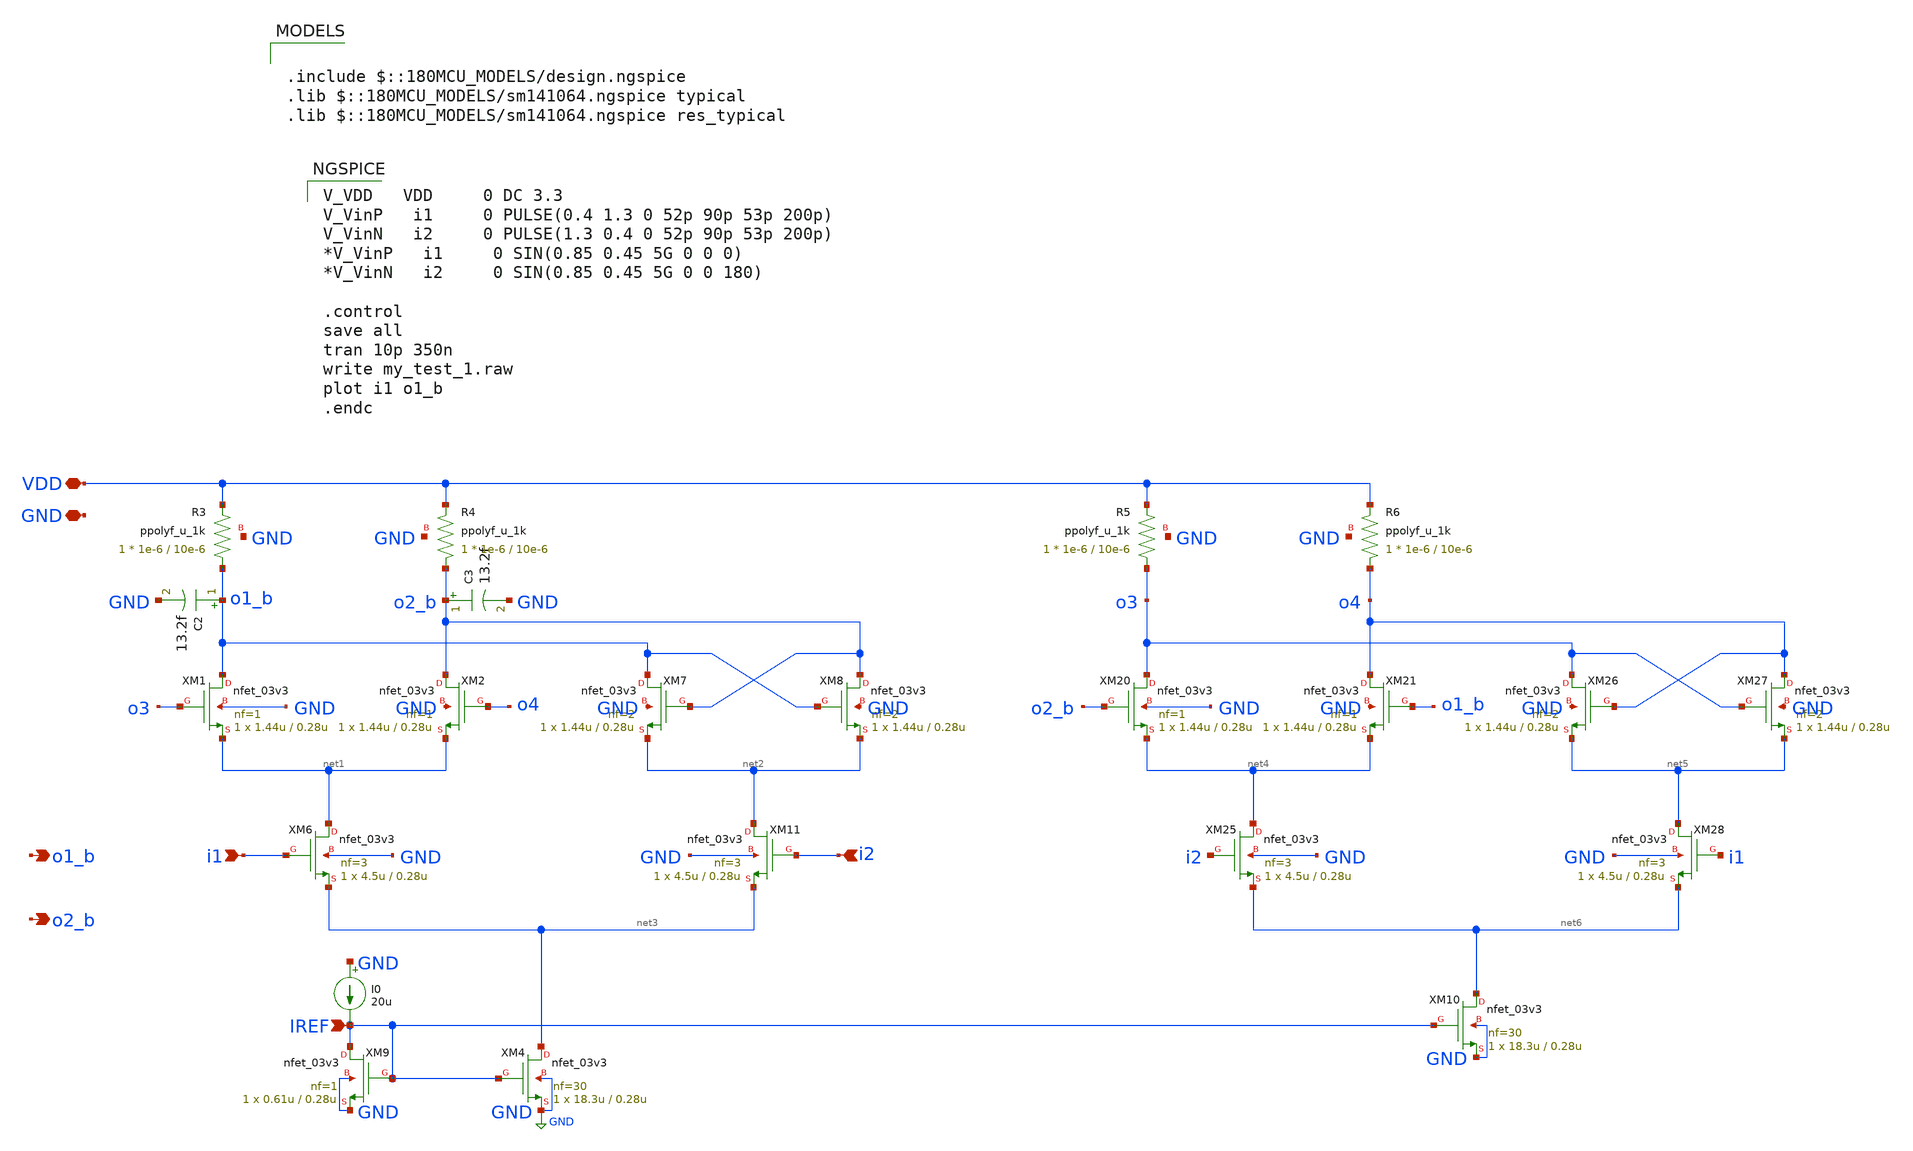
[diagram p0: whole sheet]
** sch_path: rha-vga-pll-blocks/blocks/pll/cml_div.sch
**.subckt cml_div i2 i1 o2_b o1_b VDD GND IREF
*.ipin i2
*.ipin i1
*.opin o2_b
*.opin o1_b
*.iopin VDD
*.iopin GND
*.ipin IREF
XM1 o1_b o3 net1 GND nfet_03v3 L=0.28u W=1.44u nf=1 ad='int((nf+1)/2) * W/nf * 0.18u' as='int((nf+2)/2) * W/nf * 0.18u'
+ pd='2*int((nf+1)/2) * (W/nf + 0.18u)' ps='2*int((nf+2)/2) * (W/nf + 0.18u)' nrd='0.18u / W' nrs='0.18u / W'
+ sa=0 sb=0 sd=0 m=1
XM2 o2_b o4 net1 GND nfet_03v3 L=0.28u W=1.44u nf=1 ad='int((nf+1)/2) * W/nf * 0.18u' as='int((nf+2)/2) * W/nf * 0.18u'
+ pd='2*int((nf+1)/2) * (W/nf + 0.18u)' ps='2*int((nf+2)/2) * (W/nf + 0.18u)' nrd='0.18u / W' nrs='0.18u / W'
+ sa=0 sb=0 sd=0 m=1
XM4 net3 IREF GND GND nfet_03v3 L=0.28u W=18.3u nf=30 ad='int((nf+1)/2) * W/nf * 0.18u' as='int((nf+2)/2) * W/nf * 0.18u'
+ pd='2*int((nf+1)/2) * (W/nf + 0.18u)' ps='2*int((nf+2)/2) * (W/nf + 0.18u)' nrd='0.18u / W' nrs='0.18u / W'
+ sa=0 sb=0 sd=0 m=1
XM6 net1 i1 net3 GND nfet_03v3 L=0.28u W=4.5u nf=3 ad='int((nf+1)/2) * W/nf * 0.18u' as='int((nf+2)/2) * W/nf * 0.18u'
+ pd='2*int((nf+1)/2) * (W/nf + 0.18u)' ps='2*int((nf+2)/2) * (W/nf + 0.18u)' nrd='0.18u / W' nrs='0.18u / W'
+ sa=0 sb=0 sd=0 m=1
XM7 o1_b o2_b net2 GND nfet_03v3 L=0.28u W=1.44u nf=2 ad='int((nf+1)/2) * W/nf * 0.18u' as='int((nf+2)/2) * W/nf * 0.18u'
+ pd='2*int((nf+1)/2) * (W/nf + 0.18u)' ps='2*int((nf+2)/2) * (W/nf + 0.18u)' nrd='0.18u / W' nrs='0.18u / W'
+ sa=0 sb=0 sd=0 m=1
XM8 o2_b o1_b net2 GND nfet_03v3 L=0.28u W=1.44u nf=2 ad='int((nf+1)/2) * W/nf * 0.18u' as='int((nf+2)/2) * W/nf * 0.18u'
+ pd='2*int((nf+1)/2) * (W/nf + 0.18u)' ps='2*int((nf+2)/2) * (W/nf + 0.18u)' nrd='0.18u / W' nrs='0.18u / W'
+ sa=0 sb=0 sd=0 m=1
XM11 net2 i2 net3 GND nfet_03v3 L=0.28u W=4.5u nf=3 ad='int((nf+1)/2) * W/nf * 0.18u' as='int((nf+2)/2) * W/nf * 0.18u'
+ pd='2*int((nf+1)/2) * (W/nf + 0.18u)' ps='2*int((nf+2)/2) * (W/nf + 0.18u)' nrd='0.18u / W' nrs='0.18u / W'
+ sa=0 sb=0 sd=0 m=1
XM9 IREF IREF GND GND nfet_03v3 L=0.28u W=0.61u nf=1 ad='int((nf+1)/2) * W/nf * 0.18u' as='int((nf+2)/2) * W/nf * 0.18u'
+ pd='2*int((nf+1)/2) * (W/nf + 0.18u)' ps='2*int((nf+2)/2) * (W/nf + 0.18u)' nrd='0.18u / W' nrs='0.18u / W'
+ sa=0 sb=0 sd=0 m=1
XM20 o3 o2_b net4 GND nfet_03v3 L=0.28u W=1.44u nf=1 ad='int((nf+1)/2) * W/nf * 0.18u' as='int((nf+2)/2) * W/nf * 0.18u'
+ pd='2*int((nf+1)/2) * (W/nf + 0.18u)' ps='2*int((nf+2)/2) * (W/nf + 0.18u)' nrd='0.18u / W' nrs='0.18u / W'
+ sa=0 sb=0 sd=0 m=1
XM21 o4 o1_b net4 GND nfet_03v3 L=0.28u W=1.44u nf=1 ad='int((nf+1)/2) * W/nf * 0.18u' as='int((nf+2)/2) * W/nf * 0.18u'
+ pd='2*int((nf+1)/2) * (W/nf + 0.18u)' ps='2*int((nf+2)/2) * (W/nf + 0.18u)' nrd='0.18u / W' nrs='0.18u / W'
+ sa=0 sb=0 sd=0 m=1
XM25 net4 i2 net6 GND nfet_03v3 L=0.28u W=4.5u nf=3 ad='int((nf+1)/2) * W/nf * 0.18u' as='int((nf+2)/2) * W/nf * 0.18u'
+ pd='2*int((nf+1)/2) * (W/nf + 0.18u)' ps='2*int((nf+2)/2) * (W/nf + 0.18u)' nrd='0.18u / W' nrs='0.18u / W'
+ sa=0 sb=0 sd=0 m=1
XM26 o3 o4 net5 GND nfet_03v3 L=0.28u W=1.44u nf=2 ad='int((nf+1)/2) * W/nf * 0.18u' as='int((nf+2)/2) * W/nf * 0.18u'
+ pd='2*int((nf+1)/2) * (W/nf + 0.18u)' ps='2*int((nf+2)/2) * (W/nf + 0.18u)' nrd='0.18u / W' nrs='0.18u / W'
+ sa=0 sb=0 sd=0 m=1
XM27 o4 o3 net5 GND nfet_03v3 L=0.28u W=1.44u nf=2 ad='int((nf+1)/2) * W/nf * 0.18u' as='int((nf+2)/2) * W/nf * 0.18u'
+ pd='2*int((nf+1)/2) * (W/nf + 0.18u)' ps='2*int((nf+2)/2) * (W/nf + 0.18u)' nrd='0.18u / W' nrs='0.18u / W'
+ sa=0 sb=0 sd=0 m=1
XM28 net5 i1 net6 GND nfet_03v3 L=0.28u W=4.5u nf=3 ad='int((nf+1)/2) * W/nf * 0.18u' as='int((nf+2)/2) * W/nf * 0.18u'
+ pd='2*int((nf+1)/2) * (W/nf + 0.18u)' ps='2*int((nf+2)/2) * (W/nf + 0.18u)' nrd='0.18u / W' nrs='0.18u / W'
+ sa=0 sb=0 sd=0 m=1
XM10 net6 IREF GND GND nfet_03v3 L=0.28u W=18.3u nf=30 ad='int((nf+1)/2) * W/nf * 0.18u' as='int((nf+2)/2) * W/nf * 0.18u'
+ pd='2*int((nf+1)/2) * (W/nf + 0.18u)' ps='2*int((nf+2)/2) * (W/nf + 0.18u)' nrd='0.18u / W' nrs='0.18u / W'
+ sa=0 sb=0 sd=0 m=1
I0 GND IREF 20u
C2 o1_b GND 13.2f m=1
C3 o2_b GND 13.2f m=1
XR3 o1_b VDD GND ppolyf_u_1k r_width=1e-6 r_length=10e-6 m=1
XR4 o2_b VDD GND ppolyf_u_1k r_width=1e-6 r_length=10e-6 m=1
XR5 o3 VDD GND ppolyf_u_1k r_width=1e-6 r_length=10e-6 m=1
XR6 o4 VDD GND ppolyf_u_1k r_width=1e-6 r_length=10e-6 m=1
**** begin user architecture code

.include $::180MCU_MODELS/design.ngspice
.lib $::180MCU_MODELS/sm141064.ngspice typical
.lib $::180MCU_MODELS/sm141064.ngspice res_typical


V_VDD   VDD     0 DC 3.3
V_VinP   i1     0 PULSE(0.4 1.3 0 52p 90p 53p 200p)
V_VinN   i2     0 PULSE(1.3 0.4 0 52p 90p 53p 200p)
*V_VinP   i1     0 SIN(0.85 0.45 5G 0 0 0)
*V_VinN   i2     0 SIN(0.85 0.45 5G 0 0 180)

.control
save all
tran 10p 350n
write my_test_1.raw
plot i1 o1_b
.endc


**** end user architecture code
**.ends
.GLOBAL GND
.end
